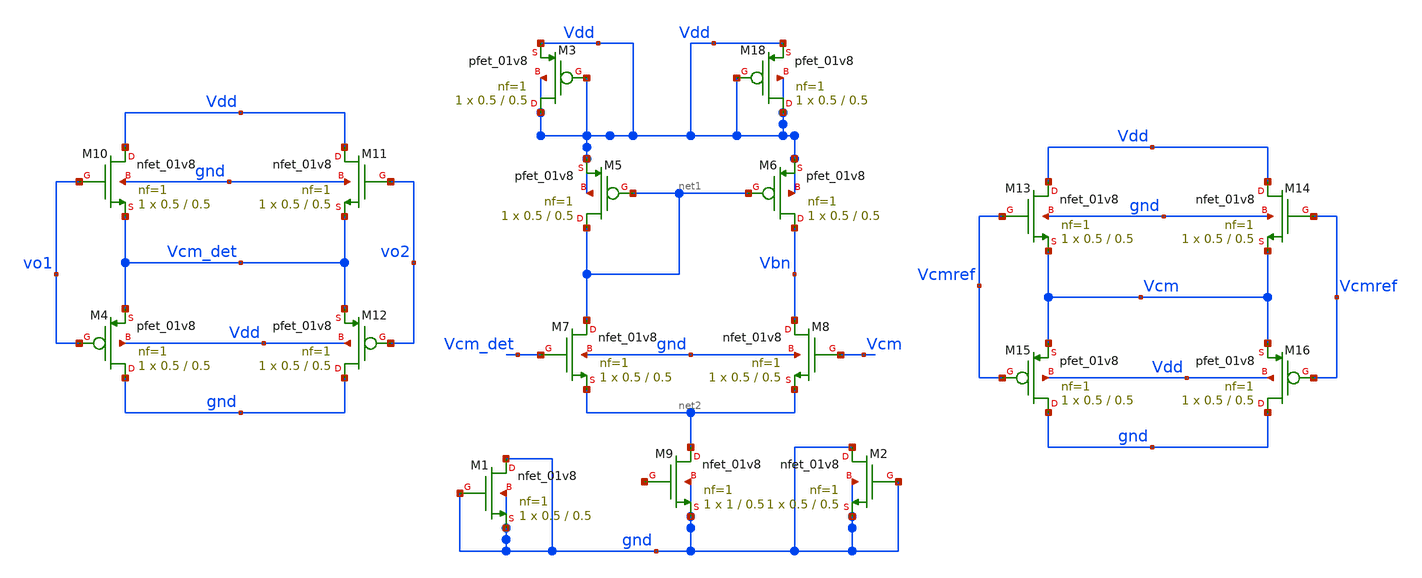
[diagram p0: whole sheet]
** sch_path: xschem/xschemfiles/cmfb.sch
**.subckt cmfb
XM4 gnd vo1 Vcm_det Vdd sky130_fd_pr__pfet_01v8 L=0.5 W=0.5 nf=1 ad='int((nf+1)/2) * W/nf * 0.29' as='int((nf+2)/2) * W/nf * 0.29'
+ pd='2*int((nf+1)/2) * (W/nf + 0.29)' ps='2*int((nf+2)/2) * (W/nf + 0.29)' nrd='0.29 / W' nrs='0.29 / W'
+ sa=0 sb=0 sd=0 mult=1 m=1
XM12 gnd vo2 Vcm_det Vdd sky130_fd_pr__pfet_01v8 L=0.5 W=0.5 nf=1 ad='int((nf+1)/2) * W/nf * 0.29' as='int((nf+2)/2) * W/nf * 0.29'
+ pd='2*int((nf+1)/2) * (W/nf + 0.29)' ps='2*int((nf+2)/2) * (W/nf + 0.29)' nrd='0.29 / W' nrs='0.29 / W'
+ sa=0 sb=0 sd=0 mult=1 m=1
XM10 Vdd vo1 Vcm_det gnd sky130_fd_pr__nfet_01v8 L=0.5 W=0.5 nf=1 ad='int((nf+1)/2) * W/nf * 0.29' as='int((nf+2)/2) * W/nf * 0.29'
+ pd='2*int((nf+1)/2) * (W/nf + 0.29)' ps='2*int((nf+2)/2) * (W/nf + 0.29)' nrd='0.29 / W' nrs='0.29 / W'
+ sa=0 sb=0 sd=0 mult=1 m=1
XM11 Vdd vo2 Vcm_det gnd sky130_fd_pr__nfet_01v8 L=0.5 W=0.5 nf=1 ad='int((nf+1)/2) * W/nf * 0.29' as='int((nf+2)/2) * W/nf * 0.29'
+ pd='2*int((nf+1)/2) * (W/nf + 0.29)' ps='2*int((nf+2)/2) * (W/nf + 0.29)' nrd='0.29 / W' nrs='0.29 / W'
+ sa=0 sb=0 sd=0 mult=1 m=1
XM5 net1 net1 Vdd Vdd sky130_fd_pr__pfet_01v8 L=0.5 W=0.5 nf=1 ad='int((nf+1)/2) * W/nf * 0.29' as='int((nf+2)/2) * W/nf * 0.29'
+ pd='2*int((nf+1)/2) * (W/nf + 0.29)' ps='2*int((nf+2)/2) * (W/nf + 0.29)' nrd='0.29 / W' nrs='0.29 / W'
+ sa=0 sb=0 sd=0 mult=1 m=1
XM6 Vbn net1 Vdd Vdd sky130_fd_pr__pfet_01v8 L=0.5 W=0.5 nf=1 ad='int((nf+1)/2) * W/nf * 0.29' as='int((nf+2)/2) * W/nf * 0.29'
+ pd='2*int((nf+1)/2) * (W/nf + 0.29)' ps='2*int((nf+2)/2) * (W/nf + 0.29)' nrd='0.29 / W' nrs='0.29 / W'
+ sa=0 sb=0 sd=0 mult=1 m=1
XM7 net1 Vcm_det net2 gnd sky130_fd_pr__nfet_01v8 L=0.5 W=0.5 nf=1 ad='int((nf+1)/2) * W/nf * 0.29' as='int((nf+2)/2) * W/nf * 0.29'
+ pd='2*int((nf+1)/2) * (W/nf + 0.29)' ps='2*int((nf+2)/2) * (W/nf + 0.29)' nrd='0.29 / W' nrs='0.29 / W'
+ sa=0 sb=0 sd=0 mult=1 m=1
XM8 Vbn Vcm net2 gnd sky130_fd_pr__nfet_01v8 L=0.5 W=0.5 nf=1 ad='int((nf+1)/2) * W/nf * 0.29' as='int((nf+2)/2) * W/nf * 0.29'
+ pd='2*int((nf+1)/2) * (W/nf + 0.29)' ps='2*int((nf+2)/2) * (W/nf + 0.29)' nrd='0.29 / W' nrs='0.29 / W'
+ sa=0 sb=0 sd=0 mult=1 m=1
XM9 net2 net3 gnd gnd sky130_fd_pr__nfet_01v8 L=0.5 W=1 nf=1 ad='int((nf+1)/2) * W/nf * 0.29' as='int((nf+2)/2) * W/nf * 0.29'
+ pd='2*int((nf+1)/2) * (W/nf + 0.29)' ps='2*int((nf+2)/2) * (W/nf + 0.29)' nrd='0.29 / W' nrs='0.29 / W'
+ sa=0 sb=0 sd=0 mult=1 m=1
XM13 Vdd Vcmref Vcm gnd sky130_fd_pr__nfet_01v8 L=0.5 W=0.5 nf=1 ad='int((nf+1)/2) * W/nf * 0.29' as='int((nf+2)/2) * W/nf * 0.29'
+ pd='2*int((nf+1)/2) * (W/nf + 0.29)' ps='2*int((nf+2)/2) * (W/nf + 0.29)' nrd='0.29 / W' nrs='0.29 / W'
+ sa=0 sb=0 sd=0 mult=1 m=1
XM14 Vdd Vcmref Vcm gnd sky130_fd_pr__nfet_01v8 L=0.5 W=0.5 nf=1 ad='int((nf+1)/2) * W/nf * 0.29' as='int((nf+2)/2) * W/nf * 0.29'
+ pd='2*int((nf+1)/2) * (W/nf + 0.29)' ps='2*int((nf+2)/2) * (W/nf + 0.29)' nrd='0.29 / W' nrs='0.29 / W'
+ sa=0 sb=0 sd=0 mult=1 m=1
XM15 gnd Vcmref Vcm Vdd sky130_fd_pr__pfet_01v8 L=0.5 W=0.5 nf=1 ad='int((nf+1)/2) * W/nf * 0.29' as='int((nf+2)/2) * W/nf * 0.29'
+ pd='2*int((nf+1)/2) * (W/nf + 0.29)' ps='2*int((nf+2)/2) * (W/nf + 0.29)' nrd='0.29 / W' nrs='0.29 / W'
+ sa=0 sb=0 sd=0 mult=1 m=1
XM16 gnd Vcmref Vcm Vdd sky130_fd_pr__pfet_01v8 L=0.5 W=0.5 nf=1 ad='int((nf+1)/2) * W/nf * 0.29' as='int((nf+2)/2) * W/nf * 0.29'
+ pd='2*int((nf+1)/2) * (W/nf + 0.29)' ps='2*int((nf+2)/2) * (W/nf + 0.29)' nrd='0.29 / W' nrs='0.29 / W'
+ sa=0 sb=0 sd=0 mult=1 m=1
XM1 gnd gnd gnd gnd sky130_fd_pr__nfet_01v8 L=0.5 W=0.5 nf=1 ad='int((nf+1)/2) * W/nf * 0.29' as='int((nf+2)/2) * W/nf * 0.29'
+ pd='2*int((nf+1)/2) * (W/nf + 0.29)' ps='2*int((nf+2)/2) * (W/nf + 0.29)' nrd='0.29 / W' nrs='0.29 / W'
+ sa=0 sb=0 sd=0 mult=1 m=1
XM2 gnd gnd gnd gnd sky130_fd_pr__nfet_01v8 L=0.5 W=0.5 nf=1 ad='int((nf+1)/2) * W/nf * 0.29' as='int((nf+2)/2) * W/nf * 0.29'
+ pd='2*int((nf+1)/2) * (W/nf + 0.29)' ps='2*int((nf+2)/2) * (W/nf + 0.29)' nrd='0.29 / W' nrs='0.29 / W'
+ sa=0 sb=0 sd=0 mult=1 m=1
XM3 Vdd Vdd Vdd Vdd sky130_fd_pr__pfet_01v8 L=0.5 W=0.5 nf=1 ad='int((nf+1)/2) * W/nf * 0.29' as='int((nf+2)/2) * W/nf * 0.29'
+ pd='2*int((nf+1)/2) * (W/nf + 0.29)' ps='2*int((nf+2)/2) * (W/nf + 0.29)' nrd='0.29 / W' nrs='0.29 / W'
+ sa=0 sb=0 sd=0 mult=1 m=1
XM18 Vdd Vdd Vdd Vdd sky130_fd_pr__pfet_01v8 L=0.5 W=0.5 nf=1 ad='int((nf+1)/2) * W/nf * 0.29' as='int((nf+2)/2) * W/nf * 0.29'
+ pd='2*int((nf+1)/2) * (W/nf + 0.29)' ps='2*int((nf+2)/2) * (W/nf + 0.29)' nrd='0.29 / W' nrs='0.29 / W'
+ sa=0 sb=0 sd=0 mult=1 m=1
**** begin user architecture code

** opencircuitdesign pdks install
.lib $::SKYWATER_MODELS/sky130.lib.spice tt


**** end user architecture code
**.ends
.end
